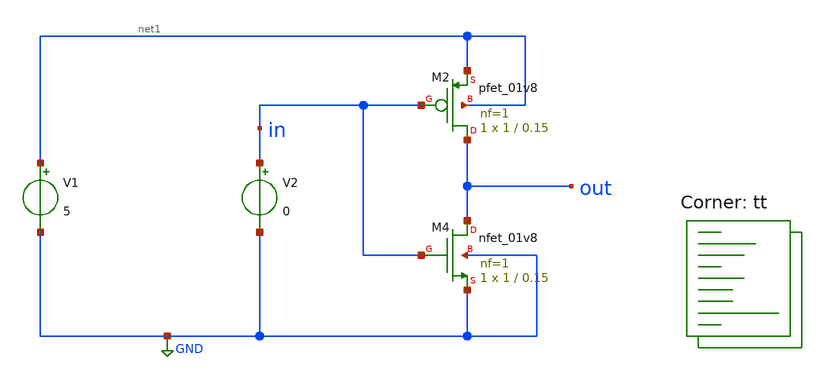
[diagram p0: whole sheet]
** sch_path: INVERTER/magic/inverter.sch
**.subckt inverter
V1 net1 GND 5
V2 in GND 0
XM2 out in net1 net1 sky130_fd_pr__pfet_01v8 L=0.15 W=1 nf=1 ad='int((nf+1)/2) * W/nf * 0.29' as='int((nf+2)/2) * W/nf * 0.29'
+ pd='2*int((nf+1)/2) * (W/nf + 0.29)' ps='2*int((nf+2)/2) * (W/nf + 0.29)' nrd='0.29 / W' nrs='0.29 / W'
+ sa=0 sb=0 sd=0 mult=1 m=1
XM4 out in GND GND sky130_fd_pr__nfet_01v8 L=0.15 W=1 nf=1 ad='int((nf+1)/2) * W/nf * 0.29' as='int((nf+2)/2) * W/nf * 0.29'
+ pd='2*int((nf+1)/2) * (W/nf + 0.29)' ps='2*int((nf+2)/2) * (W/nf + 0.29)' nrd='0.29 / W' nrs='0.29 / W'
+ sa=0 sb=0 sd=0 mult=1 m=1
**** begin user architecture code
.lib $::SKYWATER_MODELS/sky130.lib.spice tt


.control
dc V2 0 5 0.1
plot out in
.endc


**** end user architecture code
**.ends
.GLOBAL GND
.end
